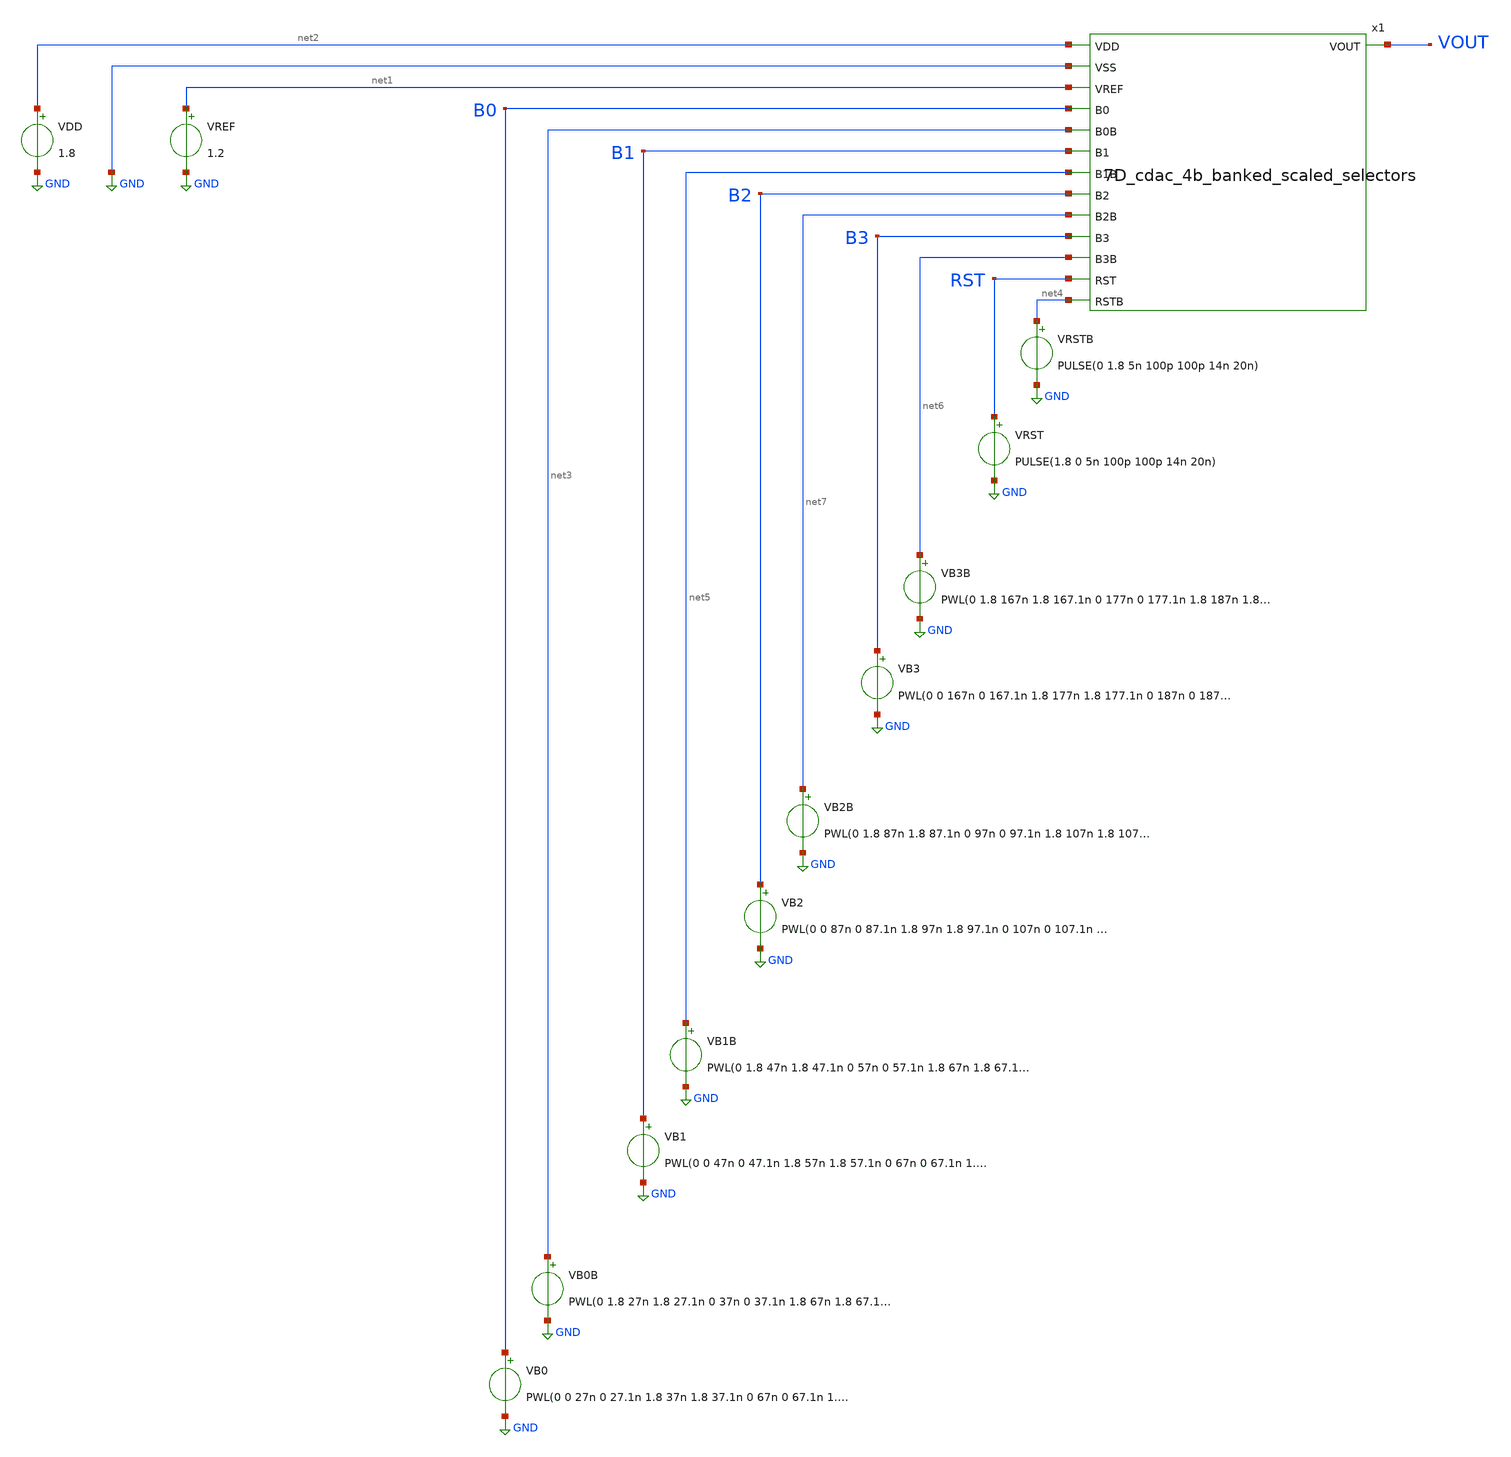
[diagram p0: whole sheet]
** sch_path: designs/libs/tb_matchmaker/tb_7D_cdac_4b_banked_scaled_selectors/tb_7D_cdac_4b_banked_scaled_selectors.sch
**.subckt tb_7D_cdac_4b_banked_scaled_selectors
VREF net1 GND 1.2
VB2B net7 GND PWL(0 1.8 87n 1.8 87.1n 0 97n 0 97.1n 1.8 107n 1.8 107.1n 0 117n 0 117.1n 1.8 127n 1.8
+ 127.1n 0 137n 0 137.1n 1.8 147n 1.8 147.1n 0 157n 0 157.1n 1.8 247n 1.8 247.1n 0 257n 0 257.1n 1.8 267n
+ 1.8 267.1n 0 277n 0 277.1n 1.8 287n 1.8 287.1n 0 297n 0 297.1n 1.8 307n 1.8 307.1n 0 317n 0 317.1n 1.8)
VB2 B2 GND PWL(0 0 87n 0 87.1n 1.8 97n 1.8 97.1n 0 107n 0 107.1n 1.8 117n 1.8 117.1n 0 127n 0 127.1n
+ 1.8 137n 1.8 137.1n 0 147n 0 147.1n 1.8 157n 1.8 157.1n 0 247n 0 247.1n 1.8 257n 1.8 257.1n 0 267n 0
+ 267.1n 1.8 277n 1.8 277.1n 0 287n 0 287.1n 1.8 297n 1.8 297.1n 0 307n 0 307.1n 1.8 317n 1.8 317.1n 0)
VDD net2 GND 1.8
VB1B net5 GND PWL(0 1.8 47n 1.8 47.1n 0 57n 0 57.1n 1.8 67n 1.8 67.1n 0 77n 0 77.1n 1.8 127n 1.8
+ 127.1n 0 137n 0 137.1n 1.8 147n 1.8 147.1n 0 157n 0 157.1n 1.8 207n 1.8 207.1n 0 217n 0 217.1n 1.8 227n
+ 1.8 227.1n 0 237n 0 237.1n 1.8 287n 1.8 287.1n 0 297n 0 297.1n 1.8 307n 1.8 307.1n 0 317n 0 317.1n 1.8)
VB1 B1 GND PWL(0 0 47n 0 47.1n 1.8 57n 1.8 57.1n 0 67n 0 67.1n 1.8 77n 1.8 77.1n 0 127n 0 127.1n 1.8
+ 137n 1.8 137.1n 0 147n 0 147.1n 1.8 157n 1.8 157.1n 0 207n 0 207.1n 1.8 217n 1.8 217.1n 0 227n 0 227.1n
+ 1.8 237n 1.8 237.1n 0 287n 0 287.1n 1.8 297n 1.8 297.1n 0 307n 0 307.1n 1.8 317n 1.8 317.1n 0)
VB0B net3 GND PWL(0 1.8 27n 1.8 27.1n 0 37n 0 37.1n 1.8 67n 1.8 67.1n 0 77n 0 77.1n 1.8 107n 1.8
+ 107.1n 0 117n 0 117.1n 1.8 147n 1.8 147.1n 0 157n 0 157.1n 1.8 187n 1.8 187.1n 0 197n 0 197.1n 1.8 227n
+ 1.8 227.1n 0 237n 0 237.1n 1.8 267n 1.8 267.1n 0 277n 0 277.1n 1.8 307n 1.8 307.1n 0 317n 0 317.1n 1.8)
VB0 B0 GND PWL(0 0 27n 0 27.1n 1.8 37n 1.8 37.1n 0 67n 0 67.1n 1.8 77n 1.8 77.1n 0 107n 0 107.1n 1.8
+ 117n 1.8 117.1n 0 147n 0 147.1n 1.8 157n 1.8 157.1n 0 187n 0 187.1n 1.8 197n 1.8 197.1n 0 227n 0 227.1n
+ 1.8 237n 1.8 237.1n 0 267n 0 267.1n 1.8 277n 1.8 277.1n 0 307n 0 307.1n 1.8 317n 1.8 317.1n 0)
VB3B net6 GND PWL(0 1.8 167n 1.8 167.1n 0 177n 0 177.1n 1.8 187n 1.8 187.1n 0 197n 0 197.1n 1.8 207n
+ 1.8 207.1n 0 217n 0 217.1n 1.8 227n 1.8 227.1n 0 237n 0 237.1n 1.8 247n 1.8 247.1n 0 257n 0 257.1n 1.8
+ 267n 1.8 267.1n 0 277n 0 277.1n 1.8 287n 1.8 287.1n 0 297n 0 297.1n 1.8 307n 1.8 307.1n 0 317n 0 317.1n
+ 1.8)
VB3 B3 GND PWL(0 0 167n 0 167.1n 1.8 177n 1.8 177.1n 0 187n 0 187.1n 1.8 197n 1.8 197.1n 0 207n 0
+ 207.1n 1.8 217n 1.8 217.1n 0 227n 0 227.1n 1.8 237n 1.8 237.1n 0 247n 0 247.1n 1.8 257n 1.8 257.1n 0 267n
+ 0 267.1n 1.8 277n 1.8 277.1n 0 287n 0 287.1n 1.8 297n 1.8 297.1n 0 307n 0 307.1n 1.8 317n 1.8 317.1n
+ 0)
VRSTB net4 GND PULSE(0 1.8 5n 100p 100p 14n 20n)
VRST RST GND PULSE(1.8 0 5n 100p 100p 14n 20n)
x1 net2 GND net1 B0 net3 B1 net5 B2 net7 B3 net6 RST VOUT net4 7D_cdac_4b_banked_scaled_selectors
**** begin user architecture code

.include /foss/pdks/gf180mcuD/libs.tech/ngspice/design.ngspice
.lib /foss/pdks/gf180mcuD/libs.tech/ngspice/sm141064.ngspice typical
.lib /foss/pdks/gf180mcuD/libs.tech/ngspice/sm141064.ngspice cap_mim
.lib /foss/pdks/gf180mcuD/libs.tech/ngspice/sm141064.ngspice mimcap_typical

.control
save all
tran 50p 320n

meas tran v0  find v(vout) at=15n
meas tran v1  find v(vout) at=35n
meas tran v2  find v(vout) at=55n
meas tran v3  find v(vout) at=75n
meas tran v4  find v(vout) at=95n
meas tran v5  find v(vout) at=115n
meas tran v6  find v(vout) at=135n
meas tran v7  find v(vout) at=155n
meas tran v8  find v(vout) at=175n
meas tran v9  find v(vout) at=195n
meas tran v10 find v(vout) at=215n
meas tran v11 find v(vout) at=235n
meas tran v12 find v(vout) at=255n
meas tran v13 find v(vout) at=275n
meas tran v14 find v(vout) at=295n
meas tran v15 find v(vout) at=315n

print v0 v1 v2 v3 v4 v5 v6 v7
print v8 v9 v10 v11 v12 v13 v14 v15
plot v(vout) v(rst)
.endc

**** end user architecture code
**.ends
.GLOBAL GND
.end
